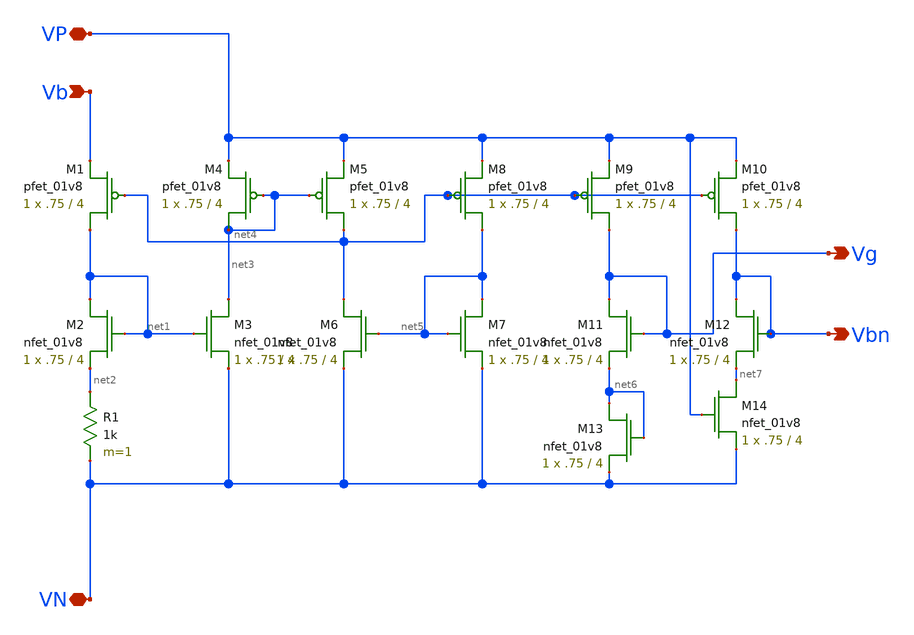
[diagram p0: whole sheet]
** sch_path: VoltageGenerator.sch
**.subckt VoltageGenerator Vb VP VN Vg Vbn
*.ipin Vb
*.iopin VP
*.iopin VN
*.opin Vg
*.opin Vbn
XM1 net1 net4 Vb VDD sky130_fd_pr__pfet_01v8 L=4 W=.75 nf=1 ad='int((nf+1)/2) * W/nf * 0.29' as='int((nf+2)/2) * W/nf * 0.29'
+ pd='2*int((nf+1)/2) * (W/nf + 0.29)' ps='2*int((nf+2)/2) * (W/nf + 0.29)' nrd='0.29 / W' nrs='0.29 / W'
+ sa=0 sb=0 sd=0 mult=1 m=1
XM2 net1 net1 net2 GND sky130_fd_pr__nfet_01v8 L=4 W=.75 nf=1 ad='int((nf+1)/2) * W/nf * 0.29' as='int((nf+2)/2) * W/nf * 0.29'
+ pd='2*int((nf+1)/2) * (W/nf + 0.29)' ps='2*int((nf+2)/2) * (W/nf + 0.29)' nrd='0.29 / W' nrs='0.29 / W'
+ sa=0 sb=0 sd=0 mult=1 m=1
XM3 net3 net1 VN GND sky130_fd_pr__nfet_01v8 L=4 W=.75 nf=1 ad='int((nf+1)/2) * W/nf * 0.29' as='int((nf+2)/2) * W/nf * 0.29'
+ pd='2*int((nf+1)/2) * (W/nf + 0.29)' ps='2*int((nf+2)/2) * (W/nf + 0.29)' nrd='0.29 / W' nrs='0.29 / W'
+ sa=0 sb=0 sd=0 mult=1 m=1
XM4 net3 net3 VP VDD sky130_fd_pr__pfet_01v8 L=4 W=.75 nf=1 ad='int((nf+1)/2) * W/nf * 0.29' as='int((nf+2)/2) * W/nf * 0.29'
+ pd='2*int((nf+1)/2) * (W/nf + 0.29)' ps='2*int((nf+2)/2) * (W/nf + 0.29)' nrd='0.29 / W' nrs='0.29 / W'
+ sa=0 sb=0 sd=0 mult=1 m=1
R1 net2 VN 1k m=1
XM5 net4 net3 VP VDD sky130_fd_pr__pfet_01v8 L=4 W=.75 nf=1 ad='int((nf+1)/2) * W/nf * 0.29' as='int((nf+2)/2) * W/nf * 0.29'
+ pd='2*int((nf+1)/2) * (W/nf + 0.29)' ps='2*int((nf+2)/2) * (W/nf + 0.29)' nrd='0.29 / W' nrs='0.29 / W'
+ sa=0 sb=0 sd=0 mult=1 m=1
XM6 net4 net5 VN GND sky130_fd_pr__nfet_01v8 L=4 W=.75 nf=1 ad='int((nf+1)/2) * W/nf * 0.29' as='int((nf+2)/2) * W/nf * 0.29'
+ pd='2*int((nf+1)/2) * (W/nf + 0.29)' ps='2*int((nf+2)/2) * (W/nf + 0.29)' nrd='0.29 / W' nrs='0.29 / W'
+ sa=0 sb=0 sd=0 mult=1 m=1
XM7 net5 net5 VN GND sky130_fd_pr__nfet_01v8 L=4 W=.75 nf=1 ad='int((nf+1)/2) * W/nf * 0.29' as='int((nf+2)/2) * W/nf * 0.29'
+ pd='2*int((nf+1)/2) * (W/nf + 0.29)' ps='2*int((nf+2)/2) * (W/nf + 0.29)' nrd='0.29 / W' nrs='0.29 / W'
+ sa=0 sb=0 sd=0 mult=1 m=1
XM8 net5 net4 VP VDD sky130_fd_pr__pfet_01v8 L=4 W=.75 nf=1 ad='int((nf+1)/2) * W/nf * 0.29' as='int((nf+2)/2) * W/nf * 0.29'
+ pd='2*int((nf+1)/2) * (W/nf + 0.29)' ps='2*int((nf+2)/2) * (W/nf + 0.29)' nrd='0.29 / W' nrs='0.29 / W'
+ sa=0 sb=0 sd=0 mult=1 m=1
XM9 Vg net4 VP VDD sky130_fd_pr__pfet_01v8 L=4 W=.75 nf=1 ad='int((nf+1)/2) * W/nf * 0.29' as='int((nf+2)/2) * W/nf * 0.29'
+ pd='2*int((nf+1)/2) * (W/nf + 0.29)' ps='2*int((nf+2)/2) * (W/nf + 0.29)' nrd='0.29 / W' nrs='0.29 / W'
+ sa=0 sb=0 sd=0 mult=1 m=1
XM10 Vbn net4 VP VDD sky130_fd_pr__pfet_01v8 L=4 W=.75 nf=1 ad='int((nf+1)/2) * W/nf * 0.29' as='int((nf+2)/2) * W/nf * 0.29'
+ pd='2*int((nf+1)/2) * (W/nf + 0.29)' ps='2*int((nf+2)/2) * (W/nf + 0.29)' nrd='0.29 / W' nrs='0.29 / W'
+ sa=0 sb=0 sd=0 mult=1 m=1
XM11 Vg Vg net6 GND sky130_fd_pr__nfet_01v8 L=4 W=.75 nf=1 ad='int((nf+1)/2) * W/nf * 0.29' as='int((nf+2)/2) * W/nf * 0.29'
+ pd='2*int((nf+1)/2) * (W/nf + 0.29)' ps='2*int((nf+2)/2) * (W/nf + 0.29)' nrd='0.29 / W' nrs='0.29 / W'
+ sa=0 sb=0 sd=0 mult=1 m=1
XM12 Vbn Vbn net7 GND sky130_fd_pr__nfet_01v8 L=4 W=.75 nf=1 ad='int((nf+1)/2) * W/nf * 0.29' as='int((nf+2)/2) * W/nf * 0.29'
+ pd='2*int((nf+1)/2) * (W/nf + 0.29)' ps='2*int((nf+2)/2) * (W/nf + 0.29)' nrd='0.29 / W' nrs='0.29 / W'
+ sa=0 sb=0 sd=0 mult=1 m=1
XM13 net6 net6 VN GND sky130_fd_pr__nfet_01v8 L=4 W=.75 nf=1 ad='int((nf+1)/2) * W/nf * 0.29' as='int((nf+2)/2) * W/nf * 0.29'
+ pd='2*int((nf+1)/2) * (W/nf + 0.29)' ps='2*int((nf+2)/2) * (W/nf + 0.29)' nrd='0.29 / W' nrs='0.29 / W'
+ sa=0 sb=0 sd=0 mult=1 m=1
XM14 net7 VP VN GND sky130_fd_pr__nfet_01v8 L=4 W=.75 nf=1 ad='int((nf+1)/2) * W/nf * 0.29' as='int((nf+2)/2) * W/nf * 0.29'
+ pd='2*int((nf+1)/2) * (W/nf + 0.29)' ps='2*int((nf+2)/2) * (W/nf + 0.29)' nrd='0.29 / W' nrs='0.29 / W'
+ sa=0 sb=0 sd=0 mult=1 m=1
**.ends
.end
